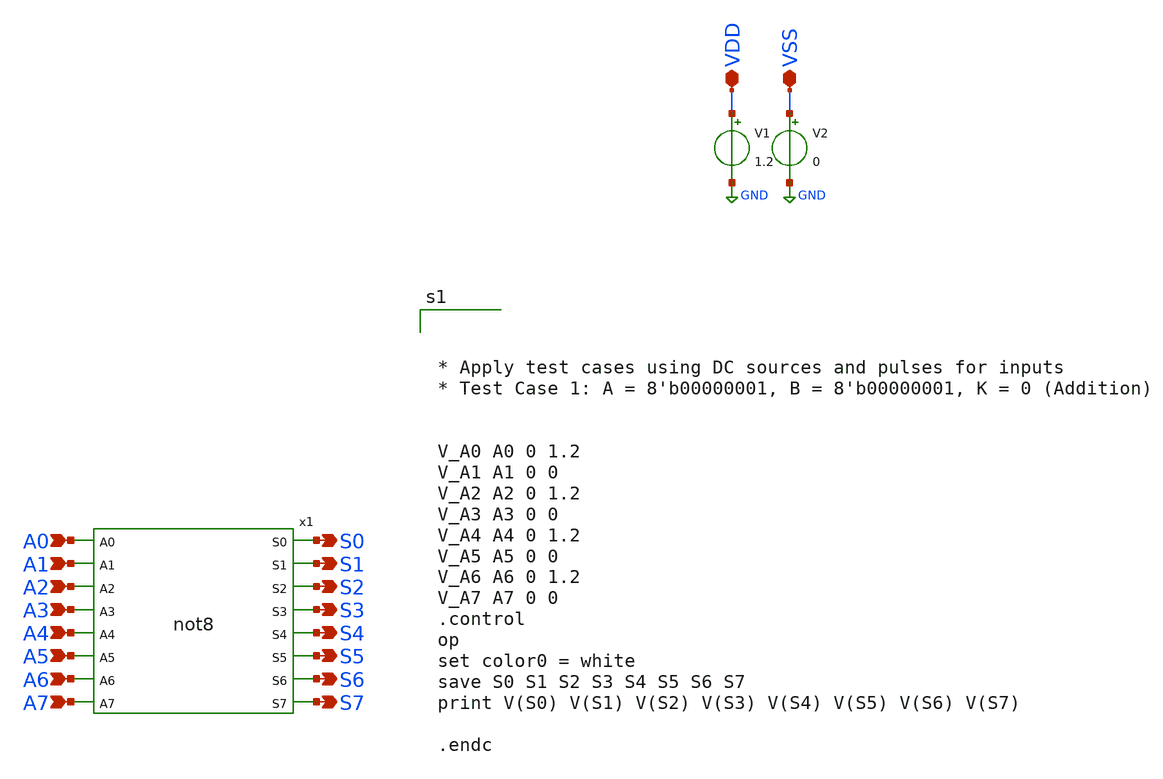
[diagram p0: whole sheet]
** sch_path: design/xschem/TEST_BENCHES/NOT8_TB.sch
**.subckt NOT8_TB A0 A1 A2 A3 A4 A5 A6 A7 S6 S7 S3 S4 S5 S0 S1 S2 VDD VSS
*.ipin A0
*.ipin A1
*.ipin A2
*.ipin A3
*.ipin A4
*.ipin A5
*.ipin A6
*.ipin A7
*.opin S6
*.opin S7
*.opin S3
*.opin S4
*.opin S5
*.opin S0
*.opin S1
*.opin S2
*.iopin VDD
*.iopin VSS
x1 A0 A1 A2 A3 A4 A5 A6 A7 S0 S1 S2 S3 S4 S5 S6 S7 not8
V1 VDD GND 1.2
V2 VSS GND 0
**** begin user architecture code

** opencircuitdesign pdks install
.lib $::SKYWATER_MODELS/sky130.lib.spice tt_mm





* Apply test cases using DC sources and pulses for inputs
* Test Case 1: A = 8'b00000001, B = 8'b00000001, K = 0 (Addition)


V_A0 A0 0 1.2
V_A1 A1 0 0
V_A2 A2 0 1.2
V_A3 A3 0 0
V_A4 A4 0 1.2
V_A5 A5 0 0
V_A6 A6 0 1.2
V_A7 A7 0 0
.control
op
set color0 = white
save S0 S1 S2 S3 S4 S5 S6 S7
print V(S0) V(S1) V(S2) V(S3) V(S4) V(S5) V(S6) V(S7)

.endc


**** end user architecture code
**.ends

* expanding   symbol:  NOT/not8.sym # of pins=16
** sym_path: design/xschem/NOT/not8.sym
** sch_path: design/xschem/NOT/not8.sch
.subckt not8 A0 A1 A2 A3 A4 A5 A6 A7 S0 S1 S2 S3 S4 S5 S6 S7
*.ipin A7
*.ipin A5
*.ipin A6
*.ipin A4
*.ipin A3
*.ipin A2
*.ipin A1
*.ipin A0
*.opin S7
*.opin S6
*.opin S5
*.opin S4
*.opin S3
*.opin S2
*.opin S1
*.opin S0
x1 A3 VSS VDD S3 inv
x2 A2 VSS VDD S2 inv
x3 A1 VSS VDD S1 inv
x4 A4 VSS VDD S4 inv
x5 A5 VSS VDD S5 inv
x6 A6 VSS VDD S6 inv
x7 A0 VSS VDD S0 inv
x9 A7 VSS VDD S7 inv
.ends


* expanding   symbol:  INV/inv.sym # of pins=2
** sym_path: design/xschem/INV/inv.sym
** sch_path: design/xschem/INV/inv.sch
.subckt inv A VSS VDD Y
*.ipin A
*.opin Y
XM2 Y A VSS GND sky130_fd_pr__nfet_01v8 L=0.15 W=1 nf=1 ad='int((nf+1)/2) * W/nf * 0.29' as='int((nf+2)/2) * W/nf * 0.29'
+ pd='2*int((nf+1)/2) * (W/nf + 0.29)' ps='2*int((nf+2)/2) * (W/nf + 0.29)' nrd='0.29 / W' nrs='0.29 / W'
+ sa=0 sb=0 sd=0 mult=1 m=1
XM1 Y A VDD VDD sky130_fd_pr__pfet_01v8 L=0.15 W=3.21 nf=1 ad='int((nf+1)/2) * W/nf * 0.29' as='int((nf+2)/2) * W/nf * 0.29'
+ pd='2*int((nf+1)/2) * (W/nf + 0.29)' ps='2*int((nf+2)/2) * (W/nf + 0.29)' nrd='0.29 / W' nrs='0.29 / W'
+ sa=0 sb=0 sd=0 mult=1 m=1
.ends

.GLOBAL GND
.end
